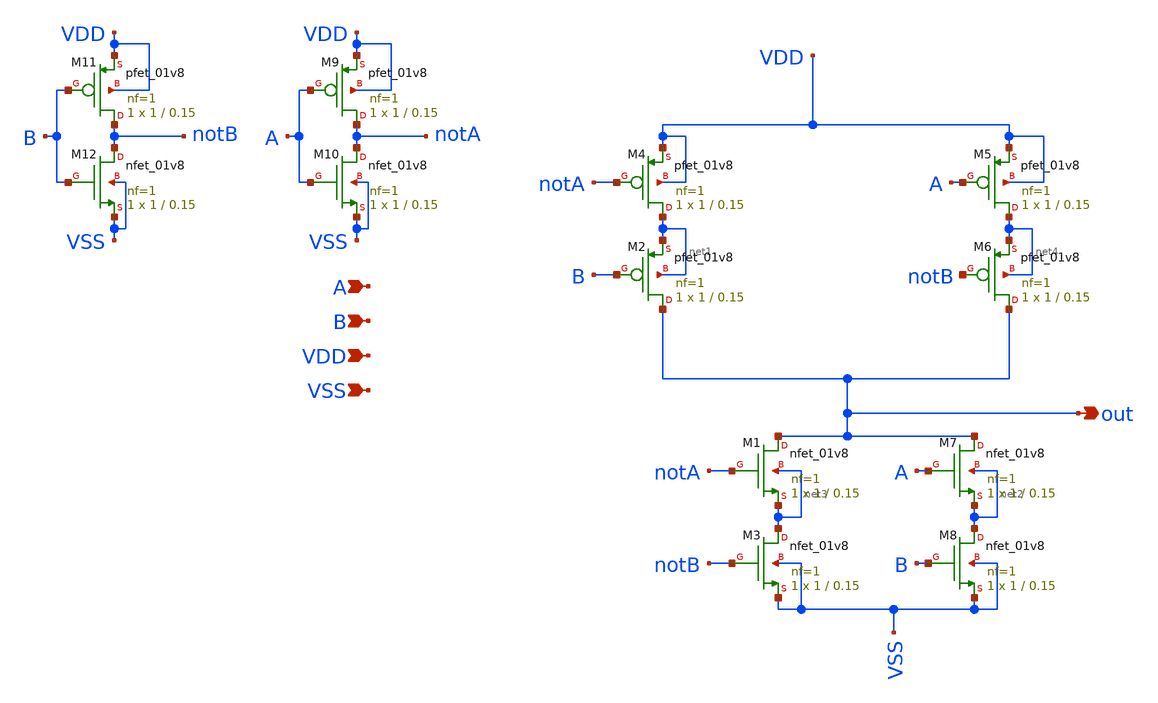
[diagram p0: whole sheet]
** sch_path: xor2/xor2.sch
**.subckt xor2 A B out VDD VSS
*.ipin A
*.ipin B
*.opin out
*.ipin VDD
*.ipin VSS
XM1 out notA net3 net3 sky130_fd_pr__nfet_01v8 L=0.15 W=1 nf=1 ad='int((nf+1)/2) * W/nf * 0.29' as='int((nf+2)/2) * W/nf * 0.29'
+ pd='2*int((nf+1)/2) * (W/nf + 0.29)' ps='2*int((nf+2)/2) * (W/nf + 0.29)' nrd='0.29 / W' nrs='0.29 / W'
+ sa=0 sb=0 sd=0 mult=1 m=1
XM2 out B net1 net1 sky130_fd_pr__pfet_01v8 L=0.15 W=1 nf=1 ad='int((nf+1)/2) * W/nf * 0.29' as='int((nf+2)/2) * W/nf * 0.29'
+ pd='2*int((nf+1)/2) * (W/nf + 0.29)' ps='2*int((nf+2)/2) * (W/nf + 0.29)' nrd='0.29 / W' nrs='0.29 / W'
+ sa=0 sb=0 sd=0 mult=1 m=1
XM3 net3 notB VSS VSS sky130_fd_pr__nfet_01v8 L=0.15 W=1 nf=1 ad='int((nf+1)/2) * W/nf * 0.29' as='int((nf+2)/2) * W/nf * 0.29'
+ pd='2*int((nf+1)/2) * (W/nf + 0.29)' ps='2*int((nf+2)/2) * (W/nf + 0.29)' nrd='0.29 / W' nrs='0.29 / W'
+ sa=0 sb=0 sd=0 mult=1 m=1
XM4 net1 notA VDD VDD sky130_fd_pr__pfet_01v8 L=0.15 W=1 nf=1 ad='int((nf+1)/2) * W/nf * 0.29' as='int((nf+2)/2) * W/nf * 0.29'
+ pd='2*int((nf+1)/2) * (W/nf + 0.29)' ps='2*int((nf+2)/2) * (W/nf + 0.29)' nrd='0.29 / W' nrs='0.29 / W'
+ sa=0 sb=0 sd=0 mult=1 m=1
XM5 net4 A VDD VDD sky130_fd_pr__pfet_01v8 L=0.15 W=1 nf=1 ad='int((nf+1)/2) * W/nf * 0.29' as='int((nf+2)/2) * W/nf * 0.29'
+ pd='2*int((nf+1)/2) * (W/nf + 0.29)' ps='2*int((nf+2)/2) * (W/nf + 0.29)' nrd='0.29 / W' nrs='0.29 / W'
+ sa=0 sb=0 sd=0 mult=1 m=1
XM6 out notB net4 net4 sky130_fd_pr__pfet_01v8 L=0.15 W=1 nf=1 ad='int((nf+1)/2) * W/nf * 0.29' as='int((nf+2)/2) * W/nf * 0.29'
+ pd='2*int((nf+1)/2) * (W/nf + 0.29)' ps='2*int((nf+2)/2) * (W/nf + 0.29)' nrd='0.29 / W' nrs='0.29 / W'
+ sa=0 sb=0 sd=0 mult=1 m=1
XM7 out A net2 net2 sky130_fd_pr__nfet_01v8 L=0.15 W=1 nf=1 ad='int((nf+1)/2) * W/nf * 0.29' as='int((nf+2)/2) * W/nf * 0.29'
+ pd='2*int((nf+1)/2) * (W/nf + 0.29)' ps='2*int((nf+2)/2) * (W/nf + 0.29)' nrd='0.29 / W' nrs='0.29 / W'
+ sa=0 sb=0 sd=0 mult=1 m=1
XM8 net2 B VSS VSS sky130_fd_pr__nfet_01v8 L=0.15 W=1 nf=1 ad='int((nf+1)/2) * W/nf * 0.29' as='int((nf+2)/2) * W/nf * 0.29'
+ pd='2*int((nf+1)/2) * (W/nf + 0.29)' ps='2*int((nf+2)/2) * (W/nf + 0.29)' nrd='0.29 / W' nrs='0.29 / W'
+ sa=0 sb=0 sd=0 mult=1 m=1
XM9 notA A VDD VDD sky130_fd_pr__pfet_01v8 L=0.15 W=1 nf=1 ad='int((nf+1)/2) * W/nf * 0.29' as='int((nf+2)/2) * W/nf * 0.29'
+ pd='2*int((nf+1)/2) * (W/nf + 0.29)' ps='2*int((nf+2)/2) * (W/nf + 0.29)' nrd='0.29 / W' nrs='0.29 / W'
+ sa=0 sb=0 sd=0 mult=1 m=1
XM10 notA A VSS VSS sky130_fd_pr__nfet_01v8 L=0.15 W=1 nf=1 ad='int((nf+1)/2) * W/nf * 0.29' as='int((nf+2)/2) * W/nf * 0.29'
+ pd='2*int((nf+1)/2) * (W/nf + 0.29)' ps='2*int((nf+2)/2) * (W/nf + 0.29)' nrd='0.29 / W' nrs='0.29 / W'
+ sa=0 sb=0 sd=0 mult=1 m=1
XM11 notB B VDD VDD sky130_fd_pr__pfet_01v8 L=0.15 W=1 nf=1 ad='int((nf+1)/2) * W/nf * 0.29' as='int((nf+2)/2) * W/nf * 0.29'
+ pd='2*int((nf+1)/2) * (W/nf + 0.29)' ps='2*int((nf+2)/2) * (W/nf + 0.29)' nrd='0.29 / W' nrs='0.29 / W'
+ sa=0 sb=0 sd=0 mult=1 m=1
XM12 notB B VSS VSS sky130_fd_pr__nfet_01v8 L=0.15 W=1 nf=1 ad='int((nf+1)/2) * W/nf * 0.29' as='int((nf+2)/2) * W/nf * 0.29'
+ pd='2*int((nf+1)/2) * (W/nf + 0.29)' ps='2*int((nf+2)/2) * (W/nf + 0.29)' nrd='0.29 / W' nrs='0.29 / W'
+ sa=0 sb=0 sd=0 mult=1 m=1
**.ends
.end
